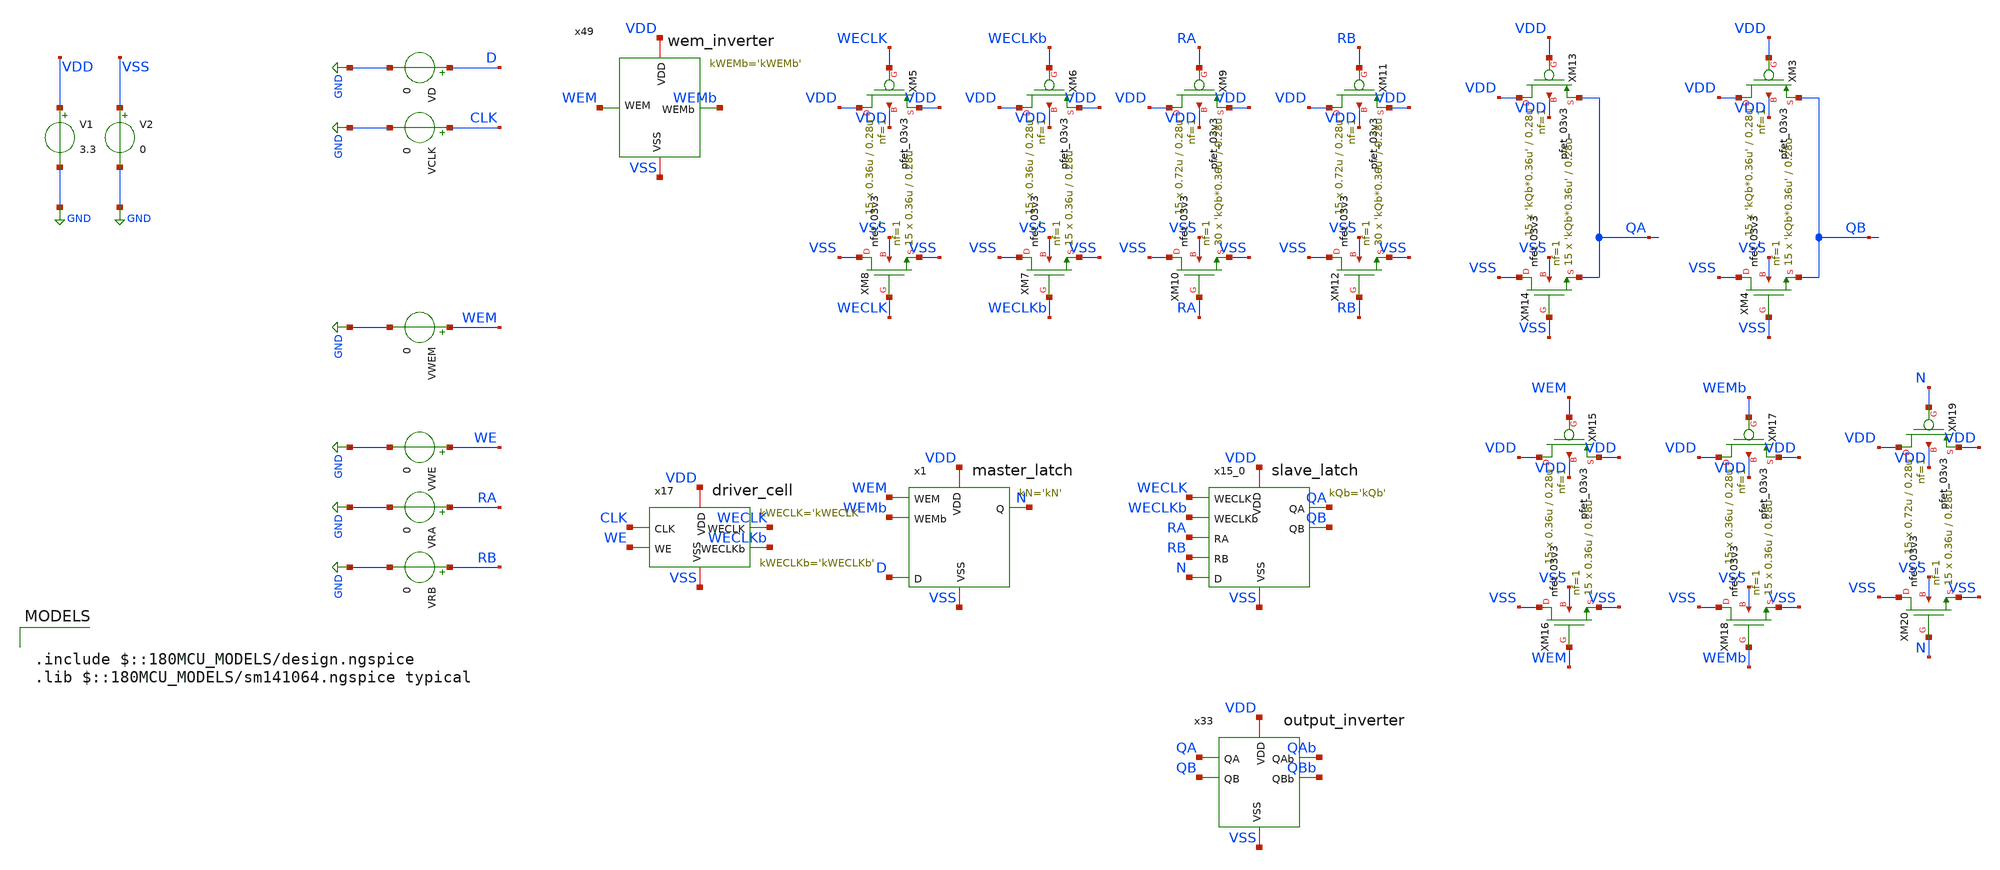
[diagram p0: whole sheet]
** sch_path: CAD3/rf_sizing_tb.sch
**.subckt rf_sizing_tb
x15_0 VDD VSS QA WECLK WECLKb RA RB QB N slave_latch kQb='kQb'
x1 VDD VSS N WEM WEMb D master_latch kN='kN'
x17 CLK WE WECLKb VDD VSS WECLK driver_cell kWECLK='kWECLK' kWECLKb='kWECLKb'
XM13 VDD VDD QA VDD pfet_03v3 L=0.28u W='kQb*0.36u' nf=1 ad='int((nf+1)/2) * W/nf * 0.18u' as='int((nf+2)/2) * W/nf * 0.18u'
+ pd='2*int((nf+1)/2) * (W/nf + 0.18u)' ps='2*int((nf+2)/2) * (W/nf + 0.18u)' nrd='0.18u / W' nrs='0.18u / W'
+ sa=0 sb=0 sd=0 m=15
XM14 VSS VSS QA VSS nfet_03v3 L=0.28u W='kQb*0.36u' nf=1 ad='int((nf+1)/2) * W/nf * 0.18u' as='int((nf+2)/2) * W/nf * 0.18u'
+ pd='2*int((nf+1)/2) * (W/nf + 0.18u)' ps='2*int((nf+2)/2) * (W/nf + 0.18u)' nrd='0.18u / W' nrs='0.18u / W'
+ sa=0 sb=0 sd=0 m=15
XM3 VDD VDD QB VDD pfet_03v3 L=0.28u W='kQb*0.36u' nf=1 ad='int((nf+1)/2) * W/nf * 0.18u' as='int((nf+2)/2) * W/nf * 0.18u'
+ pd='2*int((nf+1)/2) * (W/nf + 0.18u)' ps='2*int((nf+2)/2) * (W/nf + 0.18u)' nrd='0.18u / W' nrs='0.18u / W'
+ sa=0 sb=0 sd=0 m=15
XM4 VSS VSS QB VSS nfet_03v3 L=0.28u W='kQb*0.36u' nf=1 ad='int((nf+1)/2) * W/nf * 0.18u' as='int((nf+2)/2) * W/nf * 0.18u'
+ pd='2*int((nf+1)/2) * (W/nf + 0.18u)' ps='2*int((nf+2)/2) * (W/nf + 0.18u)' nrd='0.18u / W' nrs='0.18u / W'
+ sa=0 sb=0 sd=0 m=15
XM5 VDD WECLK VDD VDD pfet_03v3 L=0.28u W=0.36u nf=1 ad='int((nf+1)/2) * W/nf * 0.18u' as='int((nf+2)/2) * W/nf * 0.18u'
+ pd='2*int((nf+1)/2) * (W/nf + 0.18u)' ps='2*int((nf+2)/2) * (W/nf + 0.18u)' nrd='0.18u / W' nrs='0.18u / W'
+ sa=0 sb=0 sd=0 m=15
XM8 VSS WECLK VSS VSS nfet_03v3 L=0.28u W=0.36u nf=1 ad='int((nf+1)/2) * W/nf * 0.18u' as='int((nf+2)/2) * W/nf * 0.18u'
+ pd='2*int((nf+1)/2) * (W/nf + 0.18u)' ps='2*int((nf+2)/2) * (W/nf + 0.18u)' nrd='0.18u / W' nrs='0.18u / W'
+ sa=0 sb=0 sd=0 m=15
XM6 VDD WECLKb VDD VDD pfet_03v3 L=0.28u W=0.36u nf=1 ad='int((nf+1)/2) * W/nf * 0.18u' as='int((nf+2)/2) * W/nf * 0.18u'
+ pd='2*int((nf+1)/2) * (W/nf + 0.18u)' ps='2*int((nf+2)/2) * (W/nf + 0.18u)' nrd='0.18u / W' nrs='0.18u / W'
+ sa=0 sb=0 sd=0 m=15
XM7 VSS WECLKb VSS VSS nfet_03v3 L=0.28u W=0.36u nf=1 ad='int((nf+1)/2) * W/nf * 0.18u' as='int((nf+2)/2) * W/nf * 0.18u'
+ pd='2*int((nf+1)/2) * (W/nf + 0.18u)' ps='2*int((nf+2)/2) * (W/nf + 0.18u)' nrd='0.18u / W' nrs='0.18u / W'
+ sa=0 sb=0 sd=0 m=15
XM9 VDD RA VDD VDD pfet_03v3 L=0.28u W=0.72u nf=1 ad='int((nf+1)/2) * W/nf * 0.18u' as='int((nf+2)/2) * W/nf * 0.18u'
+ pd='2*int((nf+1)/2) * (W/nf + 0.18u)' ps='2*int((nf+2)/2) * (W/nf + 0.18u)' nrd='0.18u / W' nrs='0.18u / W'
+ sa=0 sb=0 sd=0 m=15
XM10 VSS RA VSS VSS nfet_03v3 L=0.28u W='kQb*0.36u' nf=1 ad='int((nf+1)/2) * W/nf * 0.18u' as='int((nf+2)/2) * W/nf * 0.18u'
+ pd='2*int((nf+1)/2) * (W/nf + 0.18u)' ps='2*int((nf+2)/2) * (W/nf + 0.18u)' nrd='0.18u / W' nrs='0.18u / W'
+ sa=0 sb=0 sd=0 m=30
XM11 VDD RB VDD VDD pfet_03v3 L=0.28u W=0.72u nf=1 ad='int((nf+1)/2) * W/nf * 0.18u' as='int((nf+2)/2) * W/nf * 0.18u'
+ pd='2*int((nf+1)/2) * (W/nf + 0.18u)' ps='2*int((nf+2)/2) * (W/nf + 0.18u)' nrd='0.18u / W' nrs='0.18u / W'
+ sa=0 sb=0 sd=0 m=15
XM12 VSS RB VSS VSS nfet_03v3 L=0.28u W='kQb*0.36u' nf=1 ad='int((nf+1)/2) * W/nf * 0.18u' as='int((nf+2)/2) * W/nf * 0.18u'
+ pd='2*int((nf+1)/2) * (W/nf + 0.18u)' ps='2*int((nf+2)/2) * (W/nf + 0.18u)' nrd='0.18u / W' nrs='0.18u / W'
+ sa=0 sb=0 sd=0 m=30
XM15 VDD WEM VDD VDD pfet_03v3 L=0.28u W=0.36u nf=1 ad='int((nf+1)/2) * W/nf * 0.18u' as='int((nf+2)/2) * W/nf * 0.18u'
+ pd='2*int((nf+1)/2) * (W/nf + 0.18u)' ps='2*int((nf+2)/2) * (W/nf + 0.18u)' nrd='0.18u / W' nrs='0.18u / W'
+ sa=0 sb=0 sd=0 m=15
XM16 VSS WEM VSS VSS nfet_03v3 L=0.28u W=0.36u nf=1 ad='int((nf+1)/2) * W/nf * 0.18u' as='int((nf+2)/2) * W/nf * 0.18u'
+ pd='2*int((nf+1)/2) * (W/nf + 0.18u)' ps='2*int((nf+2)/2) * (W/nf + 0.18u)' nrd='0.18u / W' nrs='0.18u / W'
+ sa=0 sb=0 sd=0 m=15
XM17 VDD WEMb VDD VDD pfet_03v3 L=0.28u W=0.36u nf=1 ad='int((nf+1)/2) * W/nf * 0.18u' as='int((nf+2)/2) * W/nf * 0.18u'
+ pd='2*int((nf+1)/2) * (W/nf + 0.18u)' ps='2*int((nf+2)/2) * (W/nf + 0.18u)' nrd='0.18u / W' nrs='0.18u / W'
+ sa=0 sb=0 sd=0 m=15
XM18 VSS WEMb VSS VSS nfet_03v3 L=0.28u W=0.36u nf=1 ad='int((nf+1)/2) * W/nf * 0.18u' as='int((nf+2)/2) * W/nf * 0.18u'
+ pd='2*int((nf+1)/2) * (W/nf + 0.18u)' ps='2*int((nf+2)/2) * (W/nf + 0.18u)' nrd='0.18u / W' nrs='0.18u / W'
+ sa=0 sb=0 sd=0 m=15
XM19 VDD N VDD VDD pfet_03v3 L=0.28u W=0.72u nf=1 ad='int((nf+1)/2) * W/nf * 0.18u' as='int((nf+2)/2) * W/nf * 0.18u'
+ pd='2*int((nf+1)/2) * (W/nf + 0.18u)' ps='2*int((nf+2)/2) * (W/nf + 0.18u)' nrd='0.18u / W' nrs='0.18u / W'
+ sa=0 sb=0 sd=0 m=15
XM20 VSS N VSS VSS nfet_03v3 L=0.28u W=0.36u nf=1 ad='int((nf+1)/2) * W/nf * 0.18u' as='int((nf+2)/2) * W/nf * 0.18u'
+ pd='2*int((nf+1)/2) * (W/nf + 0.18u)' ps='2*int((nf+2)/2) * (W/nf + 0.18u)' nrd='0.18u / W' nrs='0.18u / W'
+ sa=0 sb=0 sd=0 m=15
V1 VDD GND 3.3
V2 VSS GND 0
VD D GND 0
VCLK CLK GND 0
VWEM WEM GND 0
VWE WE GND 0
VRA RA GND 0
VRB RB GND 0
x33 VDD VSS QAb QA QB QBb output_inverter
x49 VDD WEM WEMb VSS wem_inverter
**** begin user architecture code


** kQb SWEEP

.param kWECLKb=1
.param kWECLK=1
.param kWEMb=1
.param kQb=1
.param kN=1

.control

** Define input signals
let f = 1e8
let T = 1/f
let PW = T/2

let DT = T * 2
let QT = T/4
let FQT = QT * 5

let tstop = 3.5 * T
let tstep = 0.001 * T
let NTRIALS = 20

compose kVALS start=1 stop=5 lin=$&NTRIALS
compose TRISE start=0 stop=0 lin=$&NTRIALS
compose TFALL start=0 stop=0 lin=$&NTRIALS

let idx = 0
while idx < NTRIALS
	let kVAL = kVALS[idx]
	alterparam kQb = $&kVAL
	reset

	** Enable WEM
	alter @VWEM[DC] = 3.3

    ** Enable WE
	alter @VWE[DC] = 3.3

	** Assert D = N
	alter @VD[PULSE] = [ 3.3 0 $&T 0 0 $&T $&DT 0 ]

    ** Assert CLK = WECLK
    alter @VCLK[PULSE] = [ 0 3.3 $&PW 0 0 $&PW $&T 0 ]

    ** Time RA
    alter @VRA[PULSE] = [ 3.3 0 $&FQT 0 0 $&PW $&T 0 ]

	tran $&tstep $&tstop
	meas tran TPLH TRIG V(RA) VAL=1.65 RISE=1 TARG V(QAb) VAL=1.65 RISE=1 TD=$&T
    meas tran TPHL TRIG V(RA) VAL=1.65 RISE=2 TARG V(QAb) VAL=1.65 FALL=1 TD=$&T
	let TRISE[idx] = $&TPLH
	let TFALL[idx] = $&TPHL
	let idx = idx + 1
end

plot TRISE vs kVALS
plot TFALL vs kVALS

let minval = minimum(TRISE)
let idxR = 0
while TRISE[idxR] > minval
  let idxR = idxR + 1
end
print kVALS[idxR]

let minval = minimum(TFALL)
let idxF = 0
while TFALL[idxF] > minval
  let idxF = idxF + 1
end
print kVALS[idxF]

.endc



.include $::180MCU_MODELS/design.ngspice
.lib $::180MCU_MODELS/sm141064.ngspice typical

**** end user architecture code
**.ends

* expanding   symbol:  engn1600-team1/CAD3/slave_latch.sym # of pins=9
** sym_path: CAD3/slave_latch.sym
** sch_path: CAD3/slave_latch.sch
.subckt slave_latch VDD VSS QA WECLK WECLKb RA RB QB D  kQb=1
*.ipin D
*.ipin RA
*.ipin RB
*.ipin WECLKb
*.ipin WECLK
*.opin QA
*.opin QB
*.iopin VDD
*.iopin VSS
XM1 net1 WECLKb net2 VDD pfet_03v3 L=0.28u W=0.36u nf=1 ad='int((nf+1)/2) * W/nf * 0.18u' as='int((nf+2)/2) * W/nf * 0.18u'
+ pd='2*int((nf+1)/2) * (W/nf + 0.18u)' ps='2*int((nf+2)/2) * (W/nf + 0.18u)' nrd='0.18u / W' nrs='0.18u / W'
+ sa=0 sb=0 sd=0 m=1
XM2 net1 D VDD VDD pfet_03v3 L=0.28u W=0.72u nf=1 ad='int((nf+1)/2) * W/nf * 0.18u' as='int((nf+2)/2) * W/nf * 0.18u'
+ pd='2*int((nf+1)/2) * (W/nf + 0.18u)' ps='2*int((nf+2)/2) * (W/nf + 0.18u)' nrd='0.18u / W' nrs='0.18u / W'
+ sa=0 sb=0 sd=0 m=1
XM3 net3 net2 VDD VDD pfet_03v3 L=0.28u W=0.72u nf=1 ad='int((nf+1)/2) * W/nf * 0.18u' as='int((nf+2)/2) * W/nf * 0.18u'
+ pd='2*int((nf+1)/2) * (W/nf + 0.18u)' ps='2*int((nf+2)/2) * (W/nf + 0.18u)' nrd='0.18u / W' nrs='0.18u / W'
+ sa=0 sb=0 sd=0 m=1
XM4 net4 net2 VDD VDD pfet_03v3 L=0.28u W=0.36u nf=1 ad='int((nf+1)/2) * W/nf * 0.18u' as='int((nf+2)/2) * W/nf * 0.18u'
+ pd='2*int((nf+1)/2) * (W/nf + 0.18u)' ps='2*int((nf+2)/2) * (W/nf + 0.18u)' nrd='0.18u / W' nrs='0.18u / W'
+ sa=0 sb=0 sd=0 m=1
XM5 VDD WECLK net8 VDD pfet_03v3 L=0.28u W=0.36u nf=1 ad='int((nf+1)/2) * W/nf * 0.18u' as='int((nf+2)/2) * W/nf * 0.18u'
+ pd='2*int((nf+1)/2) * (W/nf + 0.18u)' ps='2*int((nf+2)/2) * (W/nf + 0.18u)' nrd='0.18u / W' nrs='0.18u / W'
+ sa=0 sb=0 sd=0 m=1
XM6 net8 net4 net2 VDD pfet_03v3 L=0.28u W=0.36u nf=1 ad='int((nf+1)/2) * W/nf * 0.18u' as='int((nf+2)/2) * W/nf * 0.18u'
+ pd='2*int((nf+1)/2) * (W/nf + 0.18u)' ps='2*int((nf+2)/2) * (W/nf + 0.18u)' nrd='0.18u / W' nrs='0.18u / W'
+ sa=0 sb=0 sd=0 m=1
XM7 net1 D VSS VSS nfet_03v3 L=0.28u W=0.36u nf=1 ad='int((nf+1)/2) * W/nf * 0.18u' as='int((nf+2)/2) * W/nf * 0.18u'
+ pd='2*int((nf+1)/2) * (W/nf + 0.18u)' ps='2*int((nf+2)/2) * (W/nf + 0.18u)' nrd='0.18u / W' nrs='0.18u / W'
+ sa=0 sb=0 sd=0 m=1
XM8 net1 WECLK net2 VSS nfet_03v3 L=0.28u W=0.36u nf=1 ad='int((nf+1)/2) * W/nf * 0.18u' as='int((nf+2)/2) * W/nf * 0.18u'
+ pd='2*int((nf+1)/2) * (W/nf + 0.18u)' ps='2*int((nf+2)/2) * (W/nf + 0.18u)' nrd='0.18u / W' nrs='0.18u / W'
+ sa=0 sb=0 sd=0 m=1
XM9 net3 net2 VSS VSS nfet_03v3 L=0.28u W=0.36u nf=1 ad='int((nf+1)/2) * W/nf * 0.18u' as='int((nf+2)/2) * W/nf * 0.18u'
+ pd='2*int((nf+1)/2) * (W/nf + 0.18u)' ps='2*int((nf+2)/2) * (W/nf + 0.18u)' nrd='0.18u / W' nrs='0.18u / W'
+ sa=0 sb=0 sd=0 m=1
XM10 net4 net2 VSS VSS nfet_03v3 L=0.28u W=0.36u nf=1 ad='int((nf+1)/2) * W/nf * 0.18u' as='int((nf+2)/2) * W/nf * 0.18u'
+ pd='2*int((nf+1)/2) * (W/nf + 0.18u)' ps='2*int((nf+2)/2) * (W/nf + 0.18u)' nrd='0.18u / W' nrs='0.18u / W'
+ sa=0 sb=0 sd=0 m=1
XM11 net7 net4 net2 VSS nfet_03v3 L=0.28u W=0.36u nf=1 ad='int((nf+1)/2) * W/nf * 0.18u' as='int((nf+2)/2) * W/nf * 0.18u'
+ pd='2*int((nf+1)/2) * (W/nf + 0.18u)' ps='2*int((nf+2)/2) * (W/nf + 0.18u)' nrd='0.18u / W' nrs='0.18u / W'
+ sa=0 sb=0 sd=0 m=1
XM12 VSS WECLKb net7 VSS nfet_03v3 L=0.28u W=0.36u nf=1 ad='int((nf+1)/2) * W/nf * 0.18u' as='int((nf+2)/2) * W/nf * 0.18u'
+ pd='2*int((nf+1)/2) * (W/nf + 0.18u)' ps='2*int((nf+2)/2) * (W/nf + 0.18u)' nrd='0.18u / W' nrs='0.18u / W'
+ sa=0 sb=0 sd=0 m=1
XM13 net3 net5 QB VDD pfet_03v3 L=0.28u W='kQb*0.36u' nf=1 ad='int((nf+1)/2) * W/nf * 0.18u' as='int((nf+2)/2) * W/nf * 0.18u'
+ pd='2*int((nf+1)/2) * (W/nf + 0.18u)' ps='2*int((nf+2)/2) * (W/nf + 0.18u)' nrd='0.18u / W' nrs='0.18u / W'
+ sa=0 sb=0 sd=0 m=1
XM14 net3 RB QB VSS nfet_03v3 L=0.28u W='kQb*0.36u' nf=1 ad='int((nf+1)/2) * W/nf * 0.18u' as='int((nf+2)/2) * W/nf * 0.18u'
+ pd='2*int((nf+1)/2) * (W/nf + 0.18u)' ps='2*int((nf+2)/2) * (W/nf + 0.18u)' nrd='0.18u / W' nrs='0.18u / W'
+ sa=0 sb=0 sd=0 m=1
XM15 net5 RB VDD VDD pfet_03v3 L=0.28u W=0.72u nf=1 ad='int((nf+1)/2) * W/nf * 0.18u' as='int((nf+2)/2) * W/nf * 0.18u'
+ pd='2*int((nf+1)/2) * (W/nf + 0.18u)' ps='2*int((nf+2)/2) * (W/nf + 0.18u)' nrd='0.18u / W' nrs='0.18u / W'
+ sa=0 sb=0 sd=0 m=1
XM16 net5 RB VSS VSS nfet_03v3 L=0.28u W=0.36u nf=1 ad='int((nf+1)/2) * W/nf * 0.18u' as='int((nf+2)/2) * W/nf * 0.18u'
+ pd='2*int((nf+1)/2) * (W/nf + 0.18u)' ps='2*int((nf+2)/2) * (W/nf + 0.18u)' nrd='0.18u / W' nrs='0.18u / W'
+ sa=0 sb=0 sd=0 m=1
XM21 net3 net6 QA VDD pfet_03v3 L=0.28u W='kQb*0.36u' nf=1 ad='int((nf+1)/2) * W/nf * 0.18u' as='int((nf+2)/2) * W/nf * 0.18u'
+ pd='2*int((nf+1)/2) * (W/nf + 0.18u)' ps='2*int((nf+2)/2) * (W/nf + 0.18u)' nrd='0.18u / W' nrs='0.18u / W'
+ sa=0 sb=0 sd=0 m=1
XM22 net3 RA QA VSS nfet_03v3 L=0.28u W='kQb*0.36u' nf=1 ad='int((nf+1)/2) * W/nf * 0.18u' as='int((nf+2)/2) * W/nf * 0.18u'
+ pd='2*int((nf+1)/2) * (W/nf + 0.18u)' ps='2*int((nf+2)/2) * (W/nf + 0.18u)' nrd='0.18u / W' nrs='0.18u / W'
+ sa=0 sb=0 sd=0 m=1
XM23 net6 RA VDD VDD pfet_03v3 L=0.28u W=0.72u nf=1 ad='int((nf+1)/2) * W/nf * 0.18u' as='int((nf+2)/2) * W/nf * 0.18u'
+ pd='2*int((nf+1)/2) * (W/nf + 0.18u)' ps='2*int((nf+2)/2) * (W/nf + 0.18u)' nrd='0.18u / W' nrs='0.18u / W'
+ sa=0 sb=0 sd=0 m=1
XM24 net6 RA VSS VSS nfet_03v3 L=0.28u W=0.36u nf=1 ad='int((nf+1)/2) * W/nf * 0.18u' as='int((nf+2)/2) * W/nf * 0.18u'
+ pd='2*int((nf+1)/2) * (W/nf + 0.18u)' ps='2*int((nf+2)/2) * (W/nf + 0.18u)' nrd='0.18u / W' nrs='0.18u / W'
+ sa=0 sb=0 sd=0 m=1
**** begin user architecture code


.param kQb=1


**** end user architecture code
.ends


* expanding   symbol:  engn1600-team1/CAD3/master_latch.sym # of pins=6
** sym_path: CAD3/master_latch.sym
** sch_path: CAD3/master_latch.sch
.subckt master_latch VDD VSS Q WEM WEMb D  kN=1
*.ipin D
*.ipin WEMb
*.ipin WEM
*.iopin VSS
*.iopin VDD
*.opin Q
XM3 net1 WEMb net2 VDD pfet_03v3 L=0.28u W=0.36u nf=1 ad='int((nf+1)/2) * W/nf * 0.18u' as='int((nf+2)/2) * W/nf * 0.18u'
+ pd='2*int((nf+1)/2) * (W/nf + 0.18u)' ps='2*int((nf+2)/2) * (W/nf + 0.18u)' nrd='0.18u / W' nrs='0.18u / W'
+ sa=0 sb=0 sd=0 m=1
XM7 net1 D VDD VDD pfet_03v3 L=0.28u W=0.72u nf=1 ad='int((nf+1)/2) * W/nf * 0.18u' as='int((nf+2)/2) * W/nf * 0.18u'
+ pd='2*int((nf+1)/2) * (W/nf + 0.18u)' ps='2*int((nf+2)/2) * (W/nf + 0.18u)' nrd='0.18u / W' nrs='0.18u / W'
+ sa=0 sb=0 sd=0 m=1
XM8 Q net2 VDD VDD pfet_03v3 L=0.28u W=0.72u nf=4 ad='int((nf+1)/2) * W/nf * 0.18u' as='int((nf+2)/2) * W/nf * 0.18u'
+ pd='2*int((nf+1)/2) * (W/nf + 0.18u)' ps='2*int((nf+2)/2) * (W/nf + 0.18u)' nrd='0.18u / W' nrs='0.18u / W'
+ sa=0 sb=0 sd=0 m=1
XM9 net3 net2 VDD VDD pfet_03v3 L=0.28u W=0.36u nf=1 ad='int((nf+1)/2) * W/nf * 0.18u' as='int((nf+2)/2) * W/nf * 0.18u'
+ pd='2*int((nf+1)/2) * (W/nf + 0.18u)' ps='2*int((nf+2)/2) * (W/nf + 0.18u)' nrd='0.18u / W' nrs='0.18u / W'
+ sa=0 sb=0 sd=0 m=1
XM10 VDD WEM net5 VDD pfet_03v3 L=0.28u W=0.36u nf=1 ad='int((nf+1)/2) * W/nf * 0.18u' as='int((nf+2)/2) * W/nf * 0.18u'
+ pd='2*int((nf+1)/2) * (W/nf + 0.18u)' ps='2*int((nf+2)/2) * (W/nf + 0.18u)' nrd='0.18u / W' nrs='0.18u / W'
+ sa=0 sb=0 sd=0 m=1
XM12 net5 net3 net2 VDD pfet_03v3 L=0.28u W=0.36u nf=1 ad='int((nf+1)/2) * W/nf * 0.18u' as='int((nf+2)/2) * W/nf * 0.18u'
+ pd='2*int((nf+1)/2) * (W/nf + 0.18u)' ps='2*int((nf+2)/2) * (W/nf + 0.18u)' nrd='0.18u / W' nrs='0.18u / W'
+ sa=0 sb=0 sd=0 m=1
XM19 net1 D VSS VSS nfet_03v3 L=0.28u W=0.36u nf=1 ad='int((nf+1)/2) * W/nf * 0.18u' as='int((nf+2)/2) * W/nf * 0.18u'
+ pd='2*int((nf+1)/2) * (W/nf + 0.18u)' ps='2*int((nf+2)/2) * (W/nf + 0.18u)' nrd='0.18u / W' nrs='0.18u / W'
+ sa=0 sb=0 sd=0 m=1
XM20 net1 WEM net2 VSS nfet_03v3 L=0.28u W=0.36u nf=1 ad='int((nf+1)/2) * W/nf * 0.18u' as='int((nf+2)/2) * W/nf * 0.18u'
+ pd='2*int((nf+1)/2) * (W/nf + 0.18u)' ps='2*int((nf+2)/2) * (W/nf + 0.18u)' nrd='0.18u / W' nrs='0.18u / W'
+ sa=0 sb=0 sd=0 m=1
XM21 Q net2 VSS VSS nfet_03v3 L=0.28u W=0.36u nf=4 ad='int((nf+1)/2) * W/nf * 0.18u' as='int((nf+2)/2) * W/nf * 0.18u'
+ pd='2*int((nf+1)/2) * (W/nf + 0.18u)' ps='2*int((nf+2)/2) * (W/nf + 0.18u)' nrd='0.18u / W' nrs='0.18u / W'
+ sa=0 sb=0 sd=0 m=1
XM22 net3 net2 VSS VSS nfet_03v3 L=0.28u W=0.36u nf=1 ad='int((nf+1)/2) * W/nf * 0.18u' as='int((nf+2)/2) * W/nf * 0.18u'
+ pd='2*int((nf+1)/2) * (W/nf + 0.18u)' ps='2*int((nf+2)/2) * (W/nf + 0.18u)' nrd='0.18u / W' nrs='0.18u / W'
+ sa=0 sb=0 sd=0 m=1
XM23 net4 net3 net2 VSS nfet_03v3 L=0.28u W=0.36u nf=1 ad='int((nf+1)/2) * W/nf * 0.18u' as='int((nf+2)/2) * W/nf * 0.18u'
+ pd='2*int((nf+1)/2) * (W/nf + 0.18u)' ps='2*int((nf+2)/2) * (W/nf + 0.18u)' nrd='0.18u / W' nrs='0.18u / W'
+ sa=0 sb=0 sd=0 m=1
XM24 VSS WEMb net4 VSS nfet_03v3 L=0.28u W=0.36u nf=1 ad='int((nf+1)/2) * W/nf * 0.18u' as='int((nf+2)/2) * W/nf * 0.18u'
+ pd='2*int((nf+1)/2) * (W/nf + 0.18u)' ps='2*int((nf+2)/2) * (W/nf + 0.18u)' nrd='0.18u / W' nrs='0.18u / W'
+ sa=0 sb=0 sd=0 m=1
.ends


* expanding   symbol:  engn1600-team1/CAD3/driver_cell.sym # of pins=6
** sym_path: CAD3/driver_cell.sym
** sch_path: CAD3/driver_cell.sch
.subckt driver_cell CLK WE WECLKb VDD VSS WECLK  kWECLK=1 kWECLKb=1
*.ipin CLK
*.ipin WE
*.iopin VSS
*.iopin VDD
*.opin WECLKb
*.opin WECLK
XM13 WECLK net1 VDD VDD pfet_03v3 L=0.28u W=2.54u nf=1 ad='int((nf+1)/2) * W/nf * 0.18u' as='int((nf+2)/2) * W/nf * 0.18u'
+ pd='2*int((nf+1)/2) * (W/nf + 0.18u)' ps='2*int((nf+2)/2) * (W/nf + 0.18u)' nrd='0.18u / W' nrs='0.18u / W'
+ sa=0 sb=0 sd=0 m=1
XM14 WECLK net1 VSS VSS nfet_03v3 L=0.28u W=1.27u nf=1 ad='int((nf+1)/2) * W/nf * 0.18u' as='int((nf+2)/2) * W/nf * 0.18u'
+ pd='2*int((nf+1)/2) * (W/nf + 0.18u)' ps='2*int((nf+2)/2) * (W/nf + 0.18u)' nrd='0.18u / W' nrs='0.18u / W'
+ sa=0 sb=0 sd=0 m=1
XM1 WECLKb WECLK VDD VDD pfet_03v3 L=0.28u W=2.68u nf=1 ad='int((nf+1)/2) * W/nf * 0.18u' as='int((nf+2)/2) * W/nf * 0.18u'
+ pd='2*int((nf+1)/2) * (W/nf + 0.18u)' ps='2*int((nf+2)/2) * (W/nf + 0.18u)' nrd='0.18u / W' nrs='0.18u / W'
+ sa=0 sb=0 sd=0 m=1
XM2 WECLKb WECLK VSS VSS nfet_03v3 L=0.28u W=1.34u nf=1 ad='int((nf+1)/2) * W/nf * 0.18u' as='int((nf+2)/2) * W/nf * 0.18u'
+ pd='2*int((nf+1)/2) * (W/nf + 0.18u)' ps='2*int((nf+2)/2) * (W/nf + 0.18u)' nrd='0.18u / W' nrs='0.18u / W'
+ sa=0 sb=0 sd=0 m=1
XM3 net1 CLK VDD VDD pfet_03v3 L=0.28u W=0.72u nf=1 ad='int((nf+1)/2) * W/nf * 0.18u' as='int((nf+2)/2) * W/nf * 0.18u'
+ pd='2*int((nf+1)/2) * (W/nf + 0.18u)' ps='2*int((nf+2)/2) * (W/nf + 0.18u)' nrd='0.18u / W' nrs='0.18u / W'
+ sa=0 sb=0 sd=0 m=1
XM4 net1 WE VDD VDD pfet_03v3 L=0.28u W=0.72u nf=1 ad='int((nf+1)/2) * W/nf * 0.18u' as='int((nf+2)/2) * W/nf * 0.18u'
+ pd='2*int((nf+1)/2) * (W/nf + 0.18u)' ps='2*int((nf+2)/2) * (W/nf + 0.18u)' nrd='0.18u / W' nrs='0.18u / W'
+ sa=0 sb=0 sd=0 m=1
XM5 net2 WE VSS VSS nfet_03v3 L=0.28u W=0.72u nf=1 ad='int((nf+1)/2) * W/nf * 0.18u' as='int((nf+2)/2) * W/nf * 0.18u'
+ pd='2*int((nf+1)/2) * (W/nf + 0.18u)' ps='2*int((nf+2)/2) * (W/nf + 0.18u)' nrd='0.18u / W' nrs='0.18u / W'
+ sa=0 sb=0 sd=0 m=1
XM6 net1 CLK net2 VSS nfet_03v3 L=0.28u W=0.72u nf=1 ad='int((nf+1)/2) * W/nf * 0.18u' as='int((nf+2)/2) * W/nf * 0.18u'
+ pd='2*int((nf+1)/2) * (W/nf + 0.18u)' ps='2*int((nf+2)/2) * (W/nf + 0.18u)' nrd='0.18u / W' nrs='0.18u / W'
+ sa=0 sb=0 sd=0 m=1
.ends


* expanding   symbol:  engn1600-team1/CAD3/output_inverter.sym # of pins=6
** sym_path: CAD3/output_inverter.sym
** sch_path: CAD3/output_inverter.sch
.subckt output_inverter VDD VSS QAb QA QB QBb
*.opin QB
*.opin QA
*.iopin VDD
*.iopin VSS
*.ipin QAb
*.ipin QBb
XM3 QB QBb VDD VDD pfet_03v3 L=0.28u W=0.72u nf=1 ad='int((nf+1)/2) * W/nf * 0.18u' as='int((nf+2)/2) * W/nf * 0.18u'
+ pd='2*int((nf+1)/2) * (W/nf + 0.18u)' ps='2*int((nf+2)/2) * (W/nf + 0.18u)' nrd='0.18u / W' nrs='0.18u / W'
+ sa=0 sb=0 sd=0 m=1
XM4 QB QBb VSS VSS nfet_03v3 L=0.28u W=0.36 nf=1 ad='int((nf+1)/2) * W/nf * 0.18u' as='int((nf+2)/2) * W/nf * 0.18u'
+ pd='2*int((nf+1)/2) * (W/nf + 0.18u)' ps='2*int((nf+2)/2) * (W/nf + 0.18u)' nrd='0.18u / W' nrs='0.18u / W'
+ sa=0 sb=0 sd=0 m=1
XM35 QA QAb VDD VDD pfet_03v3 L=0.28u W=0.72u nf=1 ad='int((nf+1)/2) * W/nf * 0.18u' as='int((nf+2)/2) * W/nf * 0.18u'
+ pd='2*int((nf+1)/2) * (W/nf + 0.18u)' ps='2*int((nf+2)/2) * (W/nf + 0.18u)' nrd='0.18u / W' nrs='0.18u / W'
+ sa=0 sb=0 sd=0 m=1
XM36 QA QAb VSS VSS nfet_03v3 L=0.28u W=0.36u nf=1 ad='int((nf+1)/2) * W/nf * 0.18u' as='int((nf+2)/2) * W/nf * 0.18u'
+ pd='2*int((nf+1)/2) * (W/nf + 0.18u)' ps='2*int((nf+2)/2) * (W/nf + 0.18u)' nrd='0.18u / W' nrs='0.18u / W'
+ sa=0 sb=0 sd=0 m=1
.ends


* expanding   symbol:  engn1600-team1/CAD3/wem_inverter.sym # of pins=4
** sym_path: CAD3/wem_inverter.sym
** sch_path: CAD3/wem_inverter.sch
.subckt wem_inverter VDD WEM WEMb VSS
*.ipin WEM
*.opin WEMb
*.iopin VDD
*.iopin VSS
XM1 WEMb WEM VDD VDD pfet_03v3 L=0.28u W='kWEMb*0.72u' nf=1 ad='int((nf+1)/2) * W/nf * 0.18u' as='int((nf+2)/2) * W/nf * 0.18u'
+ pd='2*int((nf+1)/2) * (W/nf + 0.18u)' ps='2*int((nf+2)/2) * (W/nf + 0.18u)' nrd='0.18u / W' nrs='0.18u / W'
+ sa=0 sb=0 sd=0 m=1
XM2 WEMb WEM VSS VSS nfet_03v3 L=0.28u W='kWEMb*0.36u' nf=1 ad='int((nf+1)/2) * W/nf * 0.18u' as='int((nf+2)/2) * W/nf * 0.18u'
+ pd='2*int((nf+1)/2) * (W/nf + 0.18u)' ps='2*int((nf+2)/2) * (W/nf + 0.18u)' nrd='0.18u / W' nrs='0.18u / W'
+ sa=0 sb=0 sd=0 m=1
**** begin user architecture code


.param kWEMb=1


**** end user architecture code
.ends

.GLOBAL GND
.end
